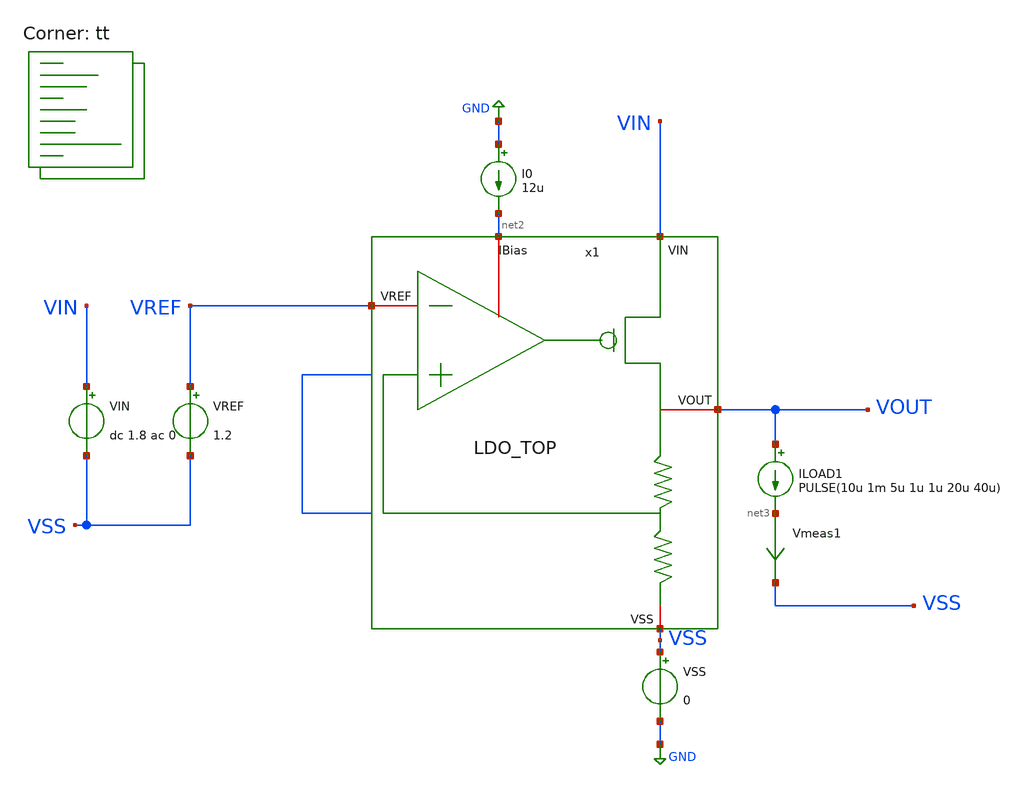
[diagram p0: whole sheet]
** sch_path: LDO_1p5V/tests/Load_tran.sch
**.subckt Load_tran
VSS VSS GND 0
VREF VREF VSS 1.2
VIN VIN VSS dc 1.8 ac 0
I0 GND net2 12u
ILOAD1 VOUT net3 PULSE(10u 1m 5u 1u 1u 20u 40u)
Vmeas1 net3 VSS 0
.save i(vmeas1)
x1 VIN net2 VREF VOUT VSS LDO_TOP
**** begin user architecture code


.options savecurrents
.save all
.save v(x1.vgate)

.control
set filetype=ascii

echo ==========================================
echo ===== LDO LOAD TRANSIENT ANALYSIS =====
echo ==========================================

op

echo ===== OPERATING POINT =====
print v(VIN)
print v(VOUT)
print v(VREF)
print v(x1.vgate)

echo ===== TRANSIENT ANALYSIS =====

* Fuente de carga en el esquemático:
* ILOAD1 PULSE(10u 1m 5u 1u 1u 20u 40u)

tran 10n 100u

echo ==========================================
echo ===== TRANSIENT MEASUREMENTS =====
echo ==========================================

* VOUT nominal = 1.5 V
* Settling band = +/-1%
* Lower band = 1.485 V
* Upper band = 1.515 V

****************************************************
* GLOBAL MIN/MAX
****************************************************

meas tran vout_min_all min v(VOUT)
meas tran vout_max_all max v(VOUT)

let global_undershoot_mv = (1.5 - vout_min_all)*1000
let global_overshoot_mv  = (vout_max_all - 1.5)*1000

****************************************************
* STEP 1: LOAD RISE 10uA -> 1mA
* Starts at 5us, ends at 6us
****************************************************

meas tran vout_min_step1 min v(VOUT) from=5u to=26u

let undershoot_step1_mv = (1.5 - vout_min_step1)*1000

* Settling after load rise:
* Time when VOUT comes back above 1.485 V
meas tran t_settle_step1_abs when v(VOUT)=1.485 rise=1 from=5u to=26u

let t_settle_step1 = t_settle_step1_abs - 5u
let t_settle_step1_us = t_settle_step1*1e6

****************************************************
* STEP 2: LOAD FALL 1mA -> 10uA
* Starts at 26us, ends at 27us
****************************************************

meas tran vout_max_step2 max v(VOUT) from=26u to=45u

let overshoot_step2_mv = (vout_max_step2 - 1.5)*1000

* Settling after load fall:
* Time when VOUT comes back below 1.515 V
meas tran t_settle_step2_abs when v(VOUT)=1.515 fall=1 from=26u to=45u

let t_settle_step2 = t_settle_step2_abs - 26u
let t_settle_step2_us = t_settle_step2*1e6

****************************************************
* STEP 3: SECOND LOAD RISE 10uA -> 1mA
* Starts at 45us, ends at 46us
****************************************************

meas tran vout_min_step3 min v(VOUT) from=45u to=66u

let undershoot_step3_mv = (1.5 - vout_min_step3)*1000

meas tran t_settle_step3_abs when v(VOUT)=1.485 rise=1 from=45u to=66u

let t_settle_step3 = t_settle_step3_abs - 45u
let t_settle_step3_us = t_settle_step3*1e6

****************************************************
* STEP 4: SECOND LOAD FALL 1mA -> 10uA
* Starts at 66us, ends at 67us
****************************************************

meas tran vout_max_step4 max v(VOUT) from=66u to=85u

let overshoot_step4_mv = (vout_max_step4 - 1.5)*1000

meas tran t_settle_step4_abs when v(VOUT)=1.515 fall=1 from=66u to=85u

let t_settle_step4 = t_settle_step4_abs - 66u
let t_settle_step4_us = t_settle_step4*1e6

****************************************************
* RESULTS
****************************************************

echo ===== GLOBAL RESULTS =====
print vout_min_all
print vout_max_all
print global_undershoot_mv
print global_overshoot_mv

echo ===== STEP 1: 10uA -> 1mA =====
print vout_min_step1
print undershoot_step1_mv
print t_settle_step1_us

echo ===== STEP 2: 1mA -> 10uA =====
print vout_max_step2
print overshoot_step2_mv
print t_settle_step2_us

echo ===== STEP 3: 10uA -> 1mA =====
print vout_min_step3
print undershoot_step3_mv
print t_settle_step3_us

echo ===== STEP 4: 1mA -> 10uA =====
print vout_max_step4
print overshoot_step4_mv
print t_settle_step4_us

****************************************************
* PLOTS
****************************************************

echo ===== PLOTS =====

plot v(VOUT)
*plot v(x1.vgate)
plot @iload1[current]
plot v(VOUT) v(x1.vgate)
*plot v(VOUT) @iload1[current]

.endc


.lib $::SKYWATER_MODELS/sky130.lib.spice tt
**** end user architecture code
**.ends

* expanding   symbol:  /foss/designs/Curso_Semiconductores/LDO_1p5V/schematics/LDO_TOP.sym # of
*+ pins=5
** sym_path: LDO/LDO_TOP.sym
** sch_path: LDO/LDO_TOP.sch
.subckt LDO_TOP VIN IBias VREF VOUT VSS
*.iopin VIN
*.iopin VREF
*.iopin IBias
*.iopin VOUT
*.iopin VSS
x1 VIN IBias VREF VOUT net1 net1 VSS LDO
.ends


* expanding   symbol:  /foss/designs/Curso_Semiconductores/LDO/LDO.sym # of pins=7
** sym_path: LDO/LDO.sym
** sch_path: LDO/LDO.sch
.subckt LDO VIN IBias VREF VOUT VFB1 VFB2 VSS
*.iopin VIN
*.iopin VREF
*.iopin VFB1
*.iopin VSS
*.iopin VFB2
*.iopin VOUT
*.iopin IBias
XM7 VOUT Vgate VIN VIN sky130_fd_pr__pfet_01v8 L=0.15 W=6 nf=1 ad='int((1 + 1)/2) * 6 / 1 * 0.29' as='int((1 + 2)/2) * 6 / 1 * 0.29'
+ pd='2*int((1 + 1)/2) * (6 / 1 + 0.29)' ps='2*int((1 + 2)/2) * (6 / 1 + 0.29)' nrd='0.29 / 6 ' nrs='0.29 / 6 '
+ sa=0 sb=0 sd=0 mult=50 m=50
XC3 Vgate VOUT sky130_fd_pr__model__cap_mim W=10 L=10 MF=1 m=1
x1 VIN Vgate VREF VFB1 IBias VSS OTA_5T
x2 VOUT VFB2 VSS RES_FB
.ends


* expanding   symbol:  /foss/designs/Curso_Semiconductores/OTA_5T/OTA_5T.sym # of pins=6
** sym_path: /foss/designs/Curso_Semiconductores/OTA_5T/OTA_5T.sym
** sch_path: /foss/designs/Curso_Semiconductores/OTA_5T/OTA_5T.sch
.subckt OTA_5T VIN VOUT_AMP VINN VINP IB VSS
*.iopin VIN
*.iopin VSS
*.iopin VOUT_AMP
*.iopin IB
*.iopin VINN
*.iopin VINP
XM1 IB IB VSS VSS sky130_fd_pr__nfet_01v8 L=1 W=2.5 nf=1 ad='int((1 + 1)/2) * 2.5 / 1 * 0.29' as='int((1 + 2)/2) * 2.5 / 1 * 0.29'
+ pd='2*int((1 + 1)/2) * (2.5 / 1 + 0.29)' ps='2*int((1 + 2)/2) * (2.5 / 1 + 0.29)' nrd='0.29 / 2.5 ' nrs='0.29 / 2.5 '
+ sa=0 sb=0 sd=0 mult=4 m=4
XM2 tail IB VSS VSS sky130_fd_pr__nfet_01v8 L=1 W=2.5 nf=1 ad='int((1 + 1)/2) * 2.5 / 1 * 0.29' as='int((1 + 2)/2) * 2.5 / 1 * 0.29'
+ pd='2*int((1 + 1)/2) * (2.5 / 1 + 0.29)' ps='2*int((1 + 2)/2) * (2.5 / 1 + 0.29)' nrd='0.29 / 2.5 ' nrs='0.29 / 2.5 '
+ sa=0 sb=0 sd=0 mult=4 m=4
XM3 net1 VINP tail VSS sky130_fd_pr__nfet_01v8 L=1 W=3 nf=1 ad='int((1 + 1)/2) * 3 / 1 * 0.29' as='int((1 + 2)/2) * 3 / 1 * 0.29'
+ pd='2*int((1 + 1)/2) * (3 / 1 + 0.29)' ps='2*int((1 + 2)/2) * (3 / 1 + 0.29)' nrd='0.29 / 3 ' nrs='0.29 / 3 '
+ sa=0 sb=0 sd=0 mult=4 m=4
XM4 VOUT_AMP VINN tail VSS sky130_fd_pr__nfet_01v8 L=1 W=3 nf=1 ad='int((1 + 1)/2) * 3 / 1 * 0.29' as='int((1 + 2)/2) * 3 / 1 * 0.29'
+ pd='2*int((1 + 1)/2) * (3 / 1 + 0.29)' ps='2*int((1 + 2)/2) * (3 / 1 + 0.29)' nrd='0.29 / 3 ' nrs='0.29 / 3 '
+ sa=0 sb=0 sd=0 mult=4 m=4
XM5 VOUT_AMP net1 VIN VIN sky130_fd_pr__pfet_01v8 L=1 W=6 nf=1 ad='int((1 + 1)/2) * 6 / 1 * 0.29' as='int((1 + 2)/2) * 6 / 1 * 0.29'
+ pd='2*int((1 + 1)/2) * (6 / 1 + 0.29)' ps='2*int((1 + 2)/2) * (6 / 1 + 0.29)' nrd='0.29 / 6 ' nrs='0.29 / 6 '
+ sa=0 sb=0 sd=0 mult=4 m=4
XM6 net1 net1 VIN VIN sky130_fd_pr__pfet_01v8 L=1 W=6 nf=1 ad='int((1 + 1)/2) * 6 / 1 * 0.29' as='int((1 + 2)/2) * 6 / 1 * 0.29'
+ pd='2*int((1 + 1)/2) * (6 / 1 + 0.29)' ps='2*int((1 + 2)/2) * (6 / 1 + 0.29)' nrd='0.29 / 6 ' nrs='0.29 / 6 '
+ sa=0 sb=0 sd=0 mult=4 m=4
XD tail VSS tail VSS sky130_fd_pr__nfet_01v8 L=0.15 W=3 nf=1 ad='int((1 + 1)/2) * 3 / 1 * 0.29' as='int((1 + 2)/2) * 3 / 1 * 0.29'
+ pd='2*int((1 + 1)/2) * (3 / 1 + 0.29)' ps='2*int((1 + 2)/2) * (3 / 1 + 0.29)' nrd='0.29 / 3 ' nrs='0.29 / 3 '
+ sa=0 sb=0 sd=0 mult=4 m=4
XM7 VIN VIN VIN VIN sky130_fd_pr__pfet_01v8 L=0.15 W=6 nf=1 ad='int((1 + 1)/2) * 6 / 1 * 0.29' as='int((1 + 2)/2) * 6 / 1 * 0.29'
+ pd='2*int((1 + 1)/2) * (6 / 1 + 0.29)' ps='2*int((1 + 2)/2) * (6 / 1 + 0.29)' nrd='0.29 / 6 ' nrs='0.29 / 6 '
+ sa=0 sb=0 sd=0 mult=4 m=4
.ends


* expanding   symbol:  /foss/designs/Curso_Semiconductores/RES_FB/RES_FB.sym # of pins=3
** sym_path: RES_FB/RES_FB.sym
** sch_path: RES_FB/RES_FB.sch
.subckt RES_FB VOUT VFB VSS
*.iopin VOUT
*.iopin VFB
*.iopin VSS
XR11 net1 VOUT VSS sky130_fd_pr__res_xhigh_po_0p69 L=8.62 mult=1 m=1
XR1 VFB net1 VSS sky130_fd_pr__res_xhigh_po_0p69 L=8.62 mult=1 m=1
XR2 net8 VFB VSS sky130_fd_pr__res_xhigh_po_0p69 L=8.62 mult=1 m=1
XR3 net4 net8 VSS sky130_fd_pr__res_xhigh_po_0p69 L=8.62 mult=1 m=1
XR4 net2 net4 VSS sky130_fd_pr__res_xhigh_po_0p69 L=8.62 mult=1 m=1
XR5 net5 net2 VSS sky130_fd_pr__res_xhigh_po_0p69 L=8.62 mult=1 m=1
XR6 net3 net5 VSS sky130_fd_pr__res_xhigh_po_0p69 L=8.62 mult=1 m=1
XR7 net7 net3 VSS sky130_fd_pr__res_xhigh_po_0p69 L=8.62 mult=1 m=1
XR8 net6 net7 VSS sky130_fd_pr__res_xhigh_po_0p69 L=8.62 mult=1 m=1
XR9 VSS net6 VSS sky130_fd_pr__res_xhigh_po_0p69 L=8.62 mult=1 m=1
.ends

.GLOBAL GND
.end
